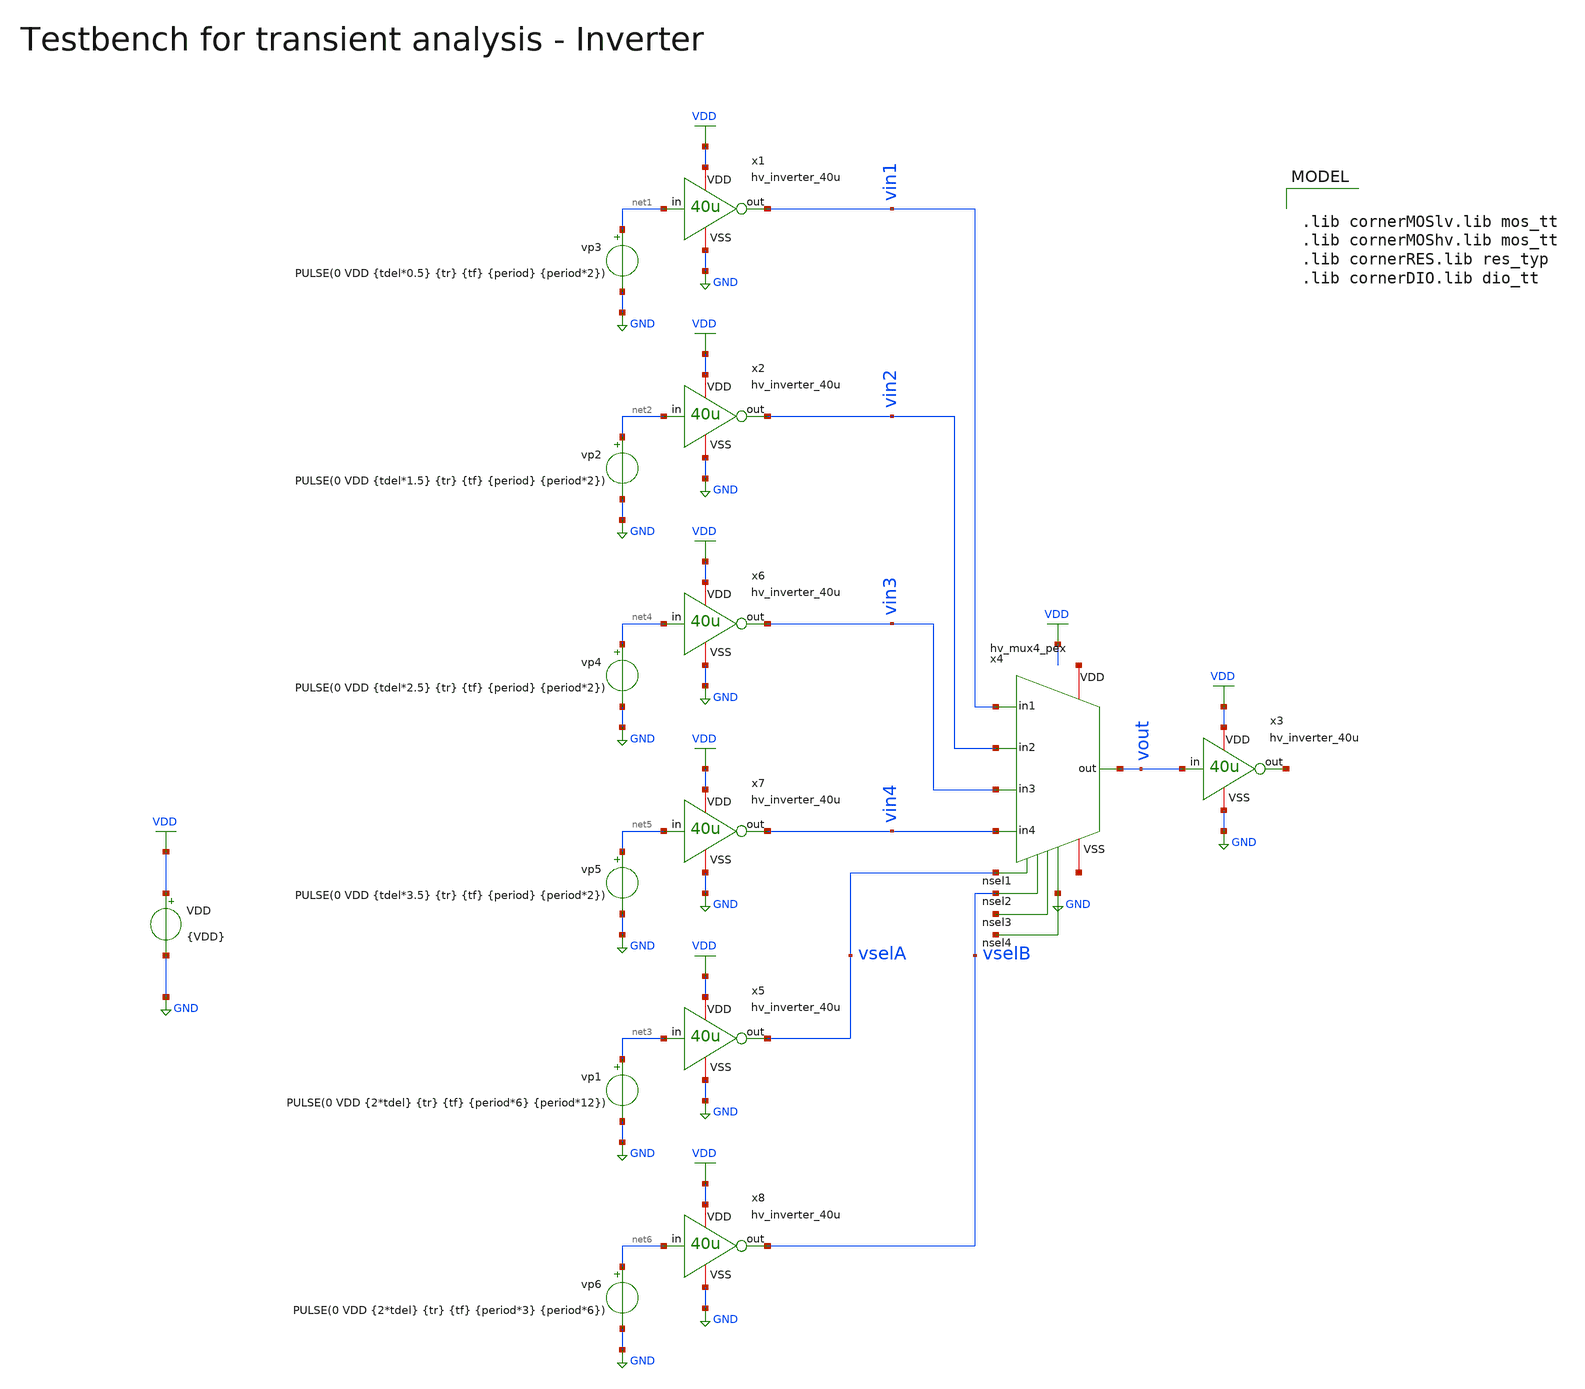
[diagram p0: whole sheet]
** sch_path: macros/heichips26_vcr/macros/switched_capacitor/testbenches/xschem/tb_hv_mux4_pex_tran.sch
**.subckt tb_hv_mux4_pex_tran
VDD VDD GND {VDD}
vp2 net2 GND PULSE(0 VDD {tdel*1.5} {tr} {tf} {period} {period*2})
vp1 net3 GND PULSE(0 VDD {2*tdel} {tr} {tf} {period*6} {period*12})
x1 VDD net1 vin1 GND hv_inverter_40u
x2 VDD net2 vin2 GND hv_inverter_40u
x3 VDD vout net7 GND hv_inverter_40u
vp3 net1 GND PULSE(0 VDD {tdel*0.5} {tr} {tf} {period} {period*2})
x5 VDD net3 vselA GND hv_inverter_40u
vp4 net4 GND PULSE(0 VDD {tdel*2.5} {tr} {tf} {period} {period*2})
x6 VDD net4 vin3 GND hv_inverter_40u
vp5 net5 GND PULSE(0 VDD {tdel*3.5} {tr} {tf} {period} {period*2})
x7 VDD net5 vin4 GND hv_inverter_40u
vp6 net6 GND PULSE(0 VDD {2*tdel} {tr} {tf} {period*3} {period*6})
x8 VDD net6 vselB GND hv_inverter_40u
x4 vselA net8 vout net9 vin3 vin1 vin4 vin2 vselB net10 net11 hv_mux4_pex
**** begin user architecture code


.include ../../../netlist/pex/hv_mux4_magic_pex_3.spice

.param VDD=3.3
.csparam VDD=VDD
.param Vcm=VDD/2
.param temp=27
.param Cload=10p
.param Rload=1k

.param period = 10n
.param tdel   = {period/4}
.param ton    = {period*2}
.csparam tstop  = {13*period}
.csparam tstep  = {period/100}
.param tr     = {period/100}
.param tf     = {period/100}

.options savecurrents klu method=gear reltol=1e-4 abstol=1e-15 gmin=1e-15
.control

save all

* Operating Point Analysis
op
remzerovec
write @schname\.raw
set appendwrite

* Transient Analysis
tran {$&tstep} {$&tstop}
write @schname\.raw

* Plotting
plot vselA+24 vselB+20 vin1+16 vin2+12 vin3+8 vin4+4 vout

* Write Data
unset appendwrite
set wr_vecnames
set wr_singlescale
wrdata ../plot_simulations/data/@schname\.txt v(vin1) v(vin2) v(vout)

*quit
.endc



.lib cornerMOSlv.lib mos_tt
.lib cornerMOShv.lib mos_tt
.lib cornerRES.lib res_typ
.lib cornerDIO.lib dio_tt

**** end user architecture code
**.ends

* expanding   symbol:  hv_inverter_40u.sym # of pins=4
** sym_path: macros/heichips26_vcr/macros/switched_capacitor/schematic/xschem/hv_inverter_40u.sym
** sch_path: macros/heichips26_vcr/macros/switched_capacitor/schematic/xschem/hv_inverter_40u.sch
.subckt hv_inverter_40u VDD in out VSS
*.ipin in
*.iopin VDD
*.iopin VSS
*.opin out
XM2 out in VSS VSS sg13_hv_nmos w={n_w} l={n_l} ng={ng} m=1 mm_ok=1
XM3 out in VDD VDD sg13_hv_pmos w={p_w} l={p_l} ng={ng} m=1 mm_ok=1
**** begin user architecture code


.param w   = 10u
.param ng  = 4
.param n_ng = ng
.param n_w = {3u*n_ng}
.param n_l = 0.45u
.param p_ng = ng
.param p_w = {10u*p_ng}
.param p_l = 0.4u


**** end user architecture code
.ends

.GLOBAL GND
.GLOBAL VDD
.end
